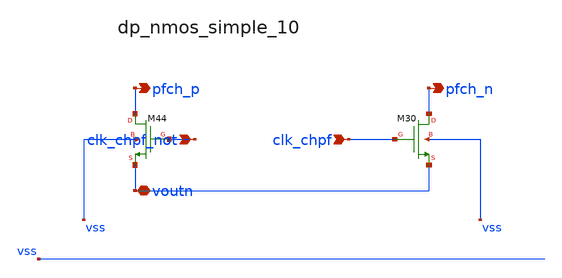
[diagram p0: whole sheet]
** sch_path: analog-db/raw/ia_003_fan_chopper_pf/hier/blocks/dp_nmos_simple_10.sch
**.subckt dp_nmos_simple_10 clk_chpf_not clk_chpf voutn pfch_p pfch_n
*.ipin clk_chpf_not
*.ipin clk_chpf
*.iopin voutn
*.opin pfch_p
*.opin pfch_n
XM30 pfch_n clk_chpf voutn vss sg13_lv_nmos w=x_dut_xm30_w l=x_dut_xm30_l ng=1 m=x_dut_xm30_m
XM44 pfch_p clk_chpf_not voutn vss sg13_lv_nmos w=x_dut_xm44_w l=x_dut_xm44_l ng=1 m=x_dut_xm44_m
**.ends
.end
